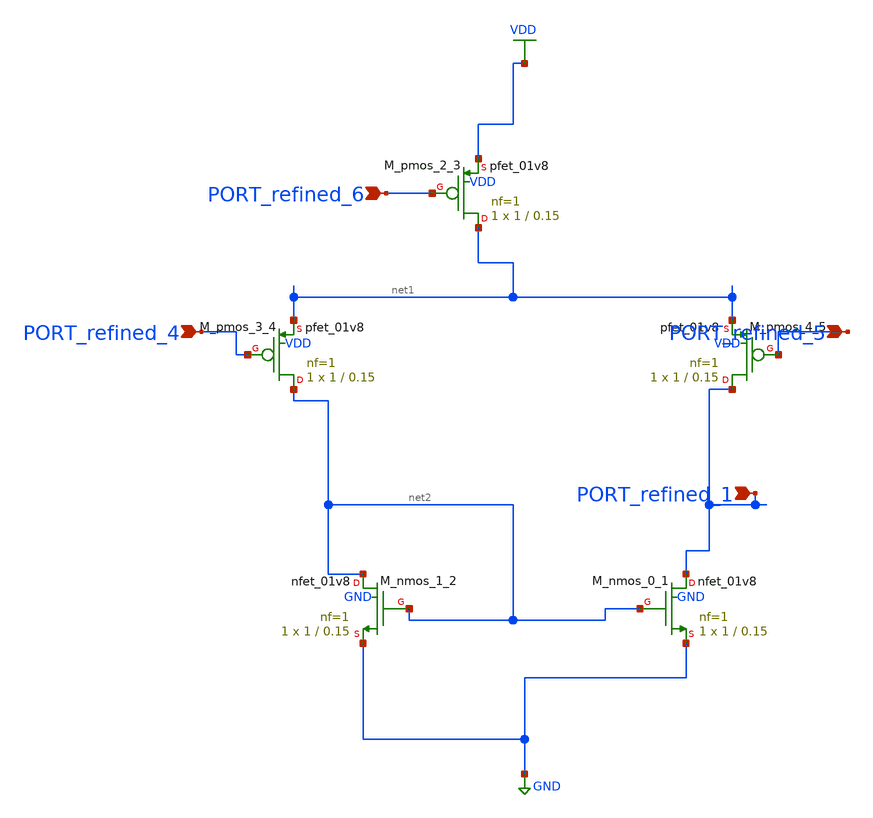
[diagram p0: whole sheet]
** sch_path: schematics/10_1109_ACCESS_2022_3157717_07_001.sch
**.subckt 10_1109_ACCESS_2022_3157717_07_001 PORT_refined_1 PORT_refined_4 PORT_refined_6
*+ PORT_refined_5
*.ipin PORT_refined_1
*.ipin PORT_refined_4
*.ipin PORT_refined_6
*.ipin PORT_refined_5
XM_nmos_0_1 PORT_refined_1 net2 GND GND sky130_fd_pr__nfet_01v8 L=0.15 W=1 nf=1 ad='int((1 + 1)/2) * 1 / 1 * 0.29'
+ as='int((1 + 2)/2) * 1 / 1 * 0.29' pd='2*int((1 + 1)/2) * (1 / 1 + 0.29)' ps='2*int((1 + 2)/2) * (1 / 1 + 0.29)'
+ nrd='0.29 / 1 ' nrs='0.29 / 1 ' sa=0 sb=0 sd=0 mult=1 m=1
XM_nmos_1_2 net2 net2 GND GND sky130_fd_pr__nfet_01v8 L=0.15 W=1 nf=1 ad='int((1 + 1)/2) * 1 / 1 * 0.29'
+ as='int((1 + 2)/2) * 1 / 1 * 0.29' pd='2*int((1 + 1)/2) * (1 / 1 + 0.29)' ps='2*int((1 + 2)/2) * (1 / 1 + 0.29)'
+ nrd='0.29 / 1 ' nrs='0.29 / 1 ' sa=0 sb=0 sd=0 mult=1 m=1
XM_pmos_2_3 net1 PORT_refined_6 VDD VDD sky130_fd_pr__pfet_01v8 L=0.15 W=1 nf=1 ad='int((1 + 1)/2) * 1 / 1 * 0.29'
+ as='int((1 + 2)/2) * 1 / 1 * 0.29' pd='2*int((1 + 1)/2) * (1 / 1 + 0.29)' ps='2*int((1 + 2)/2) * (1 / 1 + 0.29)'
+ nrd='0.29 / 1 ' nrs='0.29 / 1 ' sa=0 sb=0 sd=0 mult=1 m=1
XM_pmos_3_4 net2 PORT_refined_4 net1 VDD sky130_fd_pr__pfet_01v8 L=0.15 W=1 nf=1 ad='int((1 + 1)/2) * 1 / 1 * 0.29'
+ as='int((1 + 2)/2) * 1 / 1 * 0.29' pd='2*int((1 + 1)/2) * (1 / 1 + 0.29)' ps='2*int((1 + 2)/2) * (1 / 1 + 0.29)'
+ nrd='0.29 / 1 ' nrs='0.29 / 1 ' sa=0 sb=0 sd=0 mult=1 m=1
XM_pmos_4_5 PORT_refined_1 PORT_refined_5 net1 VDD sky130_fd_pr__pfet_01v8 L=0.15 W=1 nf=1 ad='int((1 + 1)/2) * 1 / 1 * 0.29'
+ as='int((1 + 2)/2) * 1 / 1 * 0.29' pd='2*int((1 + 1)/2) * (1 / 1 + 0.29)' ps='2*int((1 + 2)/2) * (1 / 1 + 0.29)'
+ nrd='0.29 / 1 ' nrs='0.29 / 1 ' sa=0 sb=0 sd=0 mult=1 m=1
**.ends
.GLOBAL GND
.GLOBAL VDD
.end
